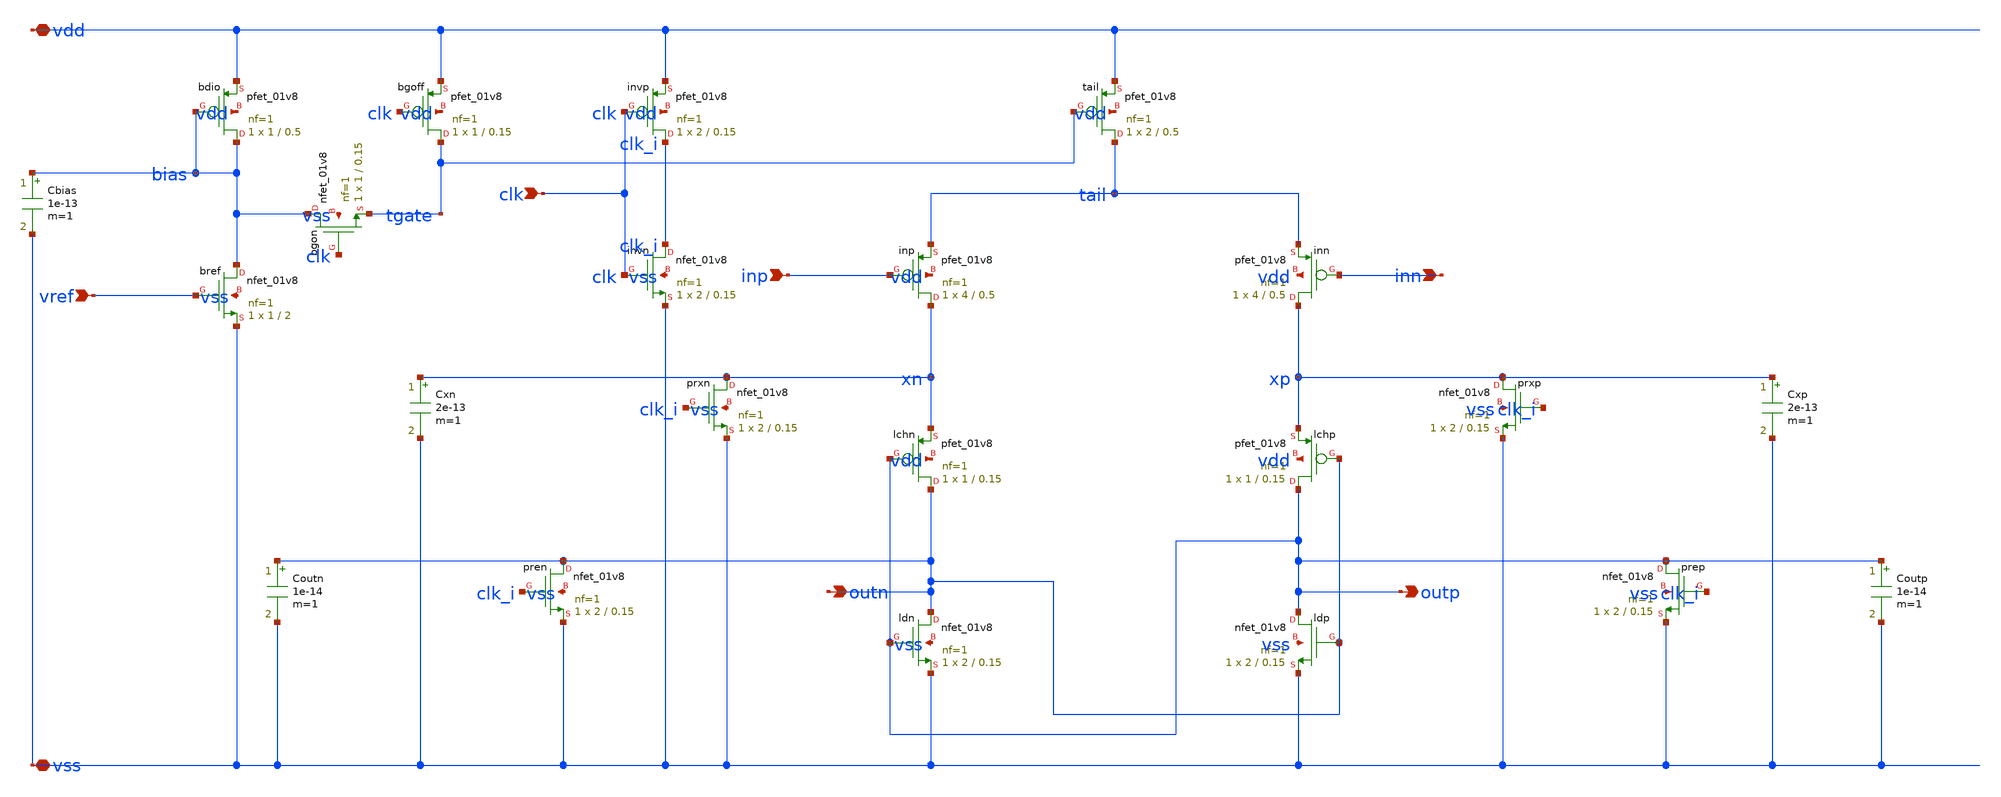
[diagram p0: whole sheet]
** sch_path: xschem/strongarm.sch
**.subckt strongarm vdd vss vref clk inp inn outp outn
*.iopin vdd
*.iopin vss
*.ipin vref
*.ipin clk
*.ipin inp
*.ipin inn
*.opin outp
*.opin outn
Cbias bias vss 1e-13 m=1
Coutn outn vss 1e-14 m=1
Coutp outp vss 1e-14 m=1
Cxn xn vss 2e-13 m=1
Cxp xp vss 2e-13 m=1
Xbdio bias bias vdd vdd sky130_fd_pr__pfet_01v8 L=0.5 W=1 nf=1 ad='int((nf+1)/2) * W/nf * 0.29' as='int((nf+2)/2) * W/nf * 0.29'
+ pd='2*int((nf+1)/2) * (W/nf + 0.29)' ps='2*int((nf+2)/2) * (W/nf + 0.29)' nrd='0.29 / W' nrs='0.29 / W'
+ sa=0 sb=0 sd=0 mult=1 m=1
Xbgoff tgate clk vdd vdd sky130_fd_pr__pfet_01v8 L=0.15 W=1 nf=1 ad='int((nf+1)/2) * W/nf * 0.29' as='int((nf+2)/2) * W/nf * 0.29'
+ pd='2*int((nf+1)/2) * (W/nf + 0.29)' ps='2*int((nf+2)/2) * (W/nf + 0.29)' nrd='0.29 / W' nrs='0.29 / W'
+ sa=0 sb=0 sd=0 mult=1 m=1
Xbgon bias clk tgate vss sky130_fd_pr__nfet_01v8 L=0.15 W=1 nf=1 ad='int((1 + 1)/2) * 1 / 1 * 0.29' as='int((1 + 2)/2) * 1 / 1 * 0.29'
+ pd='2*int((1 + 1)/2) * (1 / 1 + 0.29)' ps='2*int((1 + 2)/2) * (1 / 1 + 0.29)' nrd='0.29 / 1 ' nrs='0.29 / 1 '
+ sa=0 sb=0 sd=0 mult=1 m=1
Xbref bias vref vss vss sky130_fd_pr__nfet_01v8 L=2 W=1 nf=1 ad='int((1 + 1)/2) * 1 / 1 * 0.29' as='int((1 + 2)/2) * 1 / 1 * 0.29'
+ pd='2*int((1 + 1)/2) * (1 / 1 + 0.29)' ps='2*int((1 + 2)/2) * (1 / 1 + 0.29)' nrd='0.29 / 1 ' nrs='0.29 / 1 '
+ sa=0 sb=0 sd=0 mult=1 m=1
Xinn xp inn tail vdd sky130_fd_pr__pfet_01v8 L=0.5 W=4 nf=1 ad='int((nf+1)/2) * W/nf * 0.29' as='int((nf+2)/2) * W/nf * 0.29'
+ pd='2*int((nf+1)/2) * (W/nf + 0.29)' ps='2*int((nf+2)/2) * (W/nf + 0.29)' nrd='0.29 / W' nrs='0.29 / W'
+ sa=0 sb=0 sd=0 mult=1 m=1
Xinp xn inp tail vdd sky130_fd_pr__pfet_01v8 L=0.5 W=4 nf=1 ad='int((nf+1)/2) * W/nf * 0.29' as='int((nf+2)/2) * W/nf * 0.29'
+ pd='2*int((nf+1)/2) * (W/nf + 0.29)' ps='2*int((nf+2)/2) * (W/nf + 0.29)' nrd='0.29 / W' nrs='0.29 / W'
+ sa=0 sb=0 sd=0 mult=1 m=1
Xinvn clk_i clk vss vss sky130_fd_pr__nfet_01v8 L=0.15 W=2 nf=1 ad='int((1 + 1)/2) * 2 / 1 * 0.29' as='int((1 + 2)/2) * 2 / 1 * 0.29'
+ pd='2*int((1 + 1)/2) * (2 / 1 + 0.29)' ps='2*int((1 + 2)/2) * (2 / 1 + 0.29)' nrd='0.29 / 2 ' nrs='0.29 / 2 '
+ sa=0 sb=0 sd=0 mult=1 m=1
Xinvp clk_i clk vdd vdd sky130_fd_pr__pfet_01v8 L=0.15 W=2 nf=1 ad='int((nf+1)/2) * W/nf * 0.29' as='int((nf+2)/2) * W/nf * 0.29'
+ pd='2*int((nf+1)/2) * (W/nf + 0.29)' ps='2*int((nf+2)/2) * (W/nf + 0.29)' nrd='0.29 / W' nrs='0.29 / W'
+ sa=0 sb=0 sd=0 mult=1 m=1
Xlchn outn outp xn vdd sky130_fd_pr__pfet_01v8 L=0.15 W=1 nf=1 ad='int((nf+1)/2) * W/nf * 0.29' as='int((nf+2)/2) * W/nf * 0.29'
+ pd='2*int((nf+1)/2) * (W/nf + 0.29)' ps='2*int((nf+2)/2) * (W/nf + 0.29)' nrd='0.29 / W' nrs='0.29 / W'
+ sa=0 sb=0 sd=0 mult=1 m=1
Xlchp outp outn xp vdd sky130_fd_pr__pfet_01v8 L=0.15 W=1 nf=1 ad='int((nf+1)/2) * W/nf * 0.29' as='int((nf+2)/2) * W/nf * 0.29'
+ pd='2*int((nf+1)/2) * (W/nf + 0.29)' ps='2*int((nf+2)/2) * (W/nf + 0.29)' nrd='0.29 / W' nrs='0.29 / W'
+ sa=0 sb=0 sd=0 mult=1 m=1
Xldn outn outp vss vss sky130_fd_pr__nfet_01v8 L=0.15 W=2 nf=1 ad='int((1 + 1)/2) * 2 / 1 * 0.29' as='int((1 + 2)/2) * 2 / 1 * 0.29'
+ pd='2*int((1 + 1)/2) * (2 / 1 + 0.29)' ps='2*int((1 + 2)/2) * (2 / 1 + 0.29)' nrd='0.29 / 2 ' nrs='0.29 / 2 '
+ sa=0 sb=0 sd=0 mult=1 m=1
Xldp outp outn vss vss sky130_fd_pr__nfet_01v8 L=0.15 W=2 nf=1 ad='int((1 + 1)/2) * 2 / 1 * 0.29' as='int((1 + 2)/2) * 2 / 1 * 0.29'
+ pd='2*int((1 + 1)/2) * (2 / 1 + 0.29)' ps='2*int((1 + 2)/2) * (2 / 1 + 0.29)' nrd='0.29 / 2 ' nrs='0.29 / 2 '
+ sa=0 sb=0 sd=0 mult=1 m=1
Xpren outn clk_i vss vss sky130_fd_pr__nfet_01v8 L=0.15 W=2 nf=1 ad='int((1 + 1)/2) * 2 / 1 * 0.29' as='int((1 + 2)/2) * 2 / 1 * 0.29'
+ pd='2*int((1 + 1)/2) * (2 / 1 + 0.29)' ps='2*int((1 + 2)/2) * (2 / 1 + 0.29)' nrd='0.29 / 2 ' nrs='0.29 / 2 '
+ sa=0 sb=0 sd=0 mult=1 m=1
Xprep outp clk_i vss vss sky130_fd_pr__nfet_01v8 L=0.15 W=2 nf=1 ad='int((1 + 1)/2) * 2 / 1 * 0.29' as='int((1 + 2)/2) * 2 / 1 * 0.29'
+ pd='2*int((1 + 1)/2) * (2 / 1 + 0.29)' ps='2*int((1 + 2)/2) * (2 / 1 + 0.29)' nrd='0.29 / 2 ' nrs='0.29 / 2 '
+ sa=0 sb=0 sd=0 mult=1 m=1
Xprxn xn clk_i vss vss sky130_fd_pr__nfet_01v8 L=0.15 W=2 nf=1 ad='int((1 + 1)/2) * 2 / 1 * 0.29' as='int((1 + 2)/2) * 2 / 1 * 0.29'
+ pd='2*int((1 + 1)/2) * (2 / 1 + 0.29)' ps='2*int((1 + 2)/2) * (2 / 1 + 0.29)' nrd='0.29 / 2 ' nrs='0.29 / 2 '
+ sa=0 sb=0 sd=0 mult=1 m=1
Xprxp xp clk_i vss vss sky130_fd_pr__nfet_01v8 L=0.15 W=2 nf=1 ad='int((1 + 1)/2) * 2 / 1 * 0.29' as='int((1 + 2)/2) * 2 / 1 * 0.29'
+ pd='2*int((1 + 1)/2) * (2 / 1 + 0.29)' ps='2*int((1 + 2)/2) * (2 / 1 + 0.29)' nrd='0.29 / 2 ' nrs='0.29 / 2 '
+ sa=0 sb=0 sd=0 mult=1 m=1
Xtail tail tgate vdd vdd sky130_fd_pr__pfet_01v8 L=0.5 W=2 nf=1 ad='int((nf+1)/2) * W/nf * 0.29' as='int((nf+2)/2) * W/nf * 0.29'
+ pd='2*int((nf+1)/2) * (W/nf + 0.29)' ps='2*int((nf+2)/2) * (W/nf + 0.29)' nrd='0.29 / W' nrs='0.29 / W'
+ sa=0 sb=0 sd=0 mult=1 m=1
**.ends
.end
